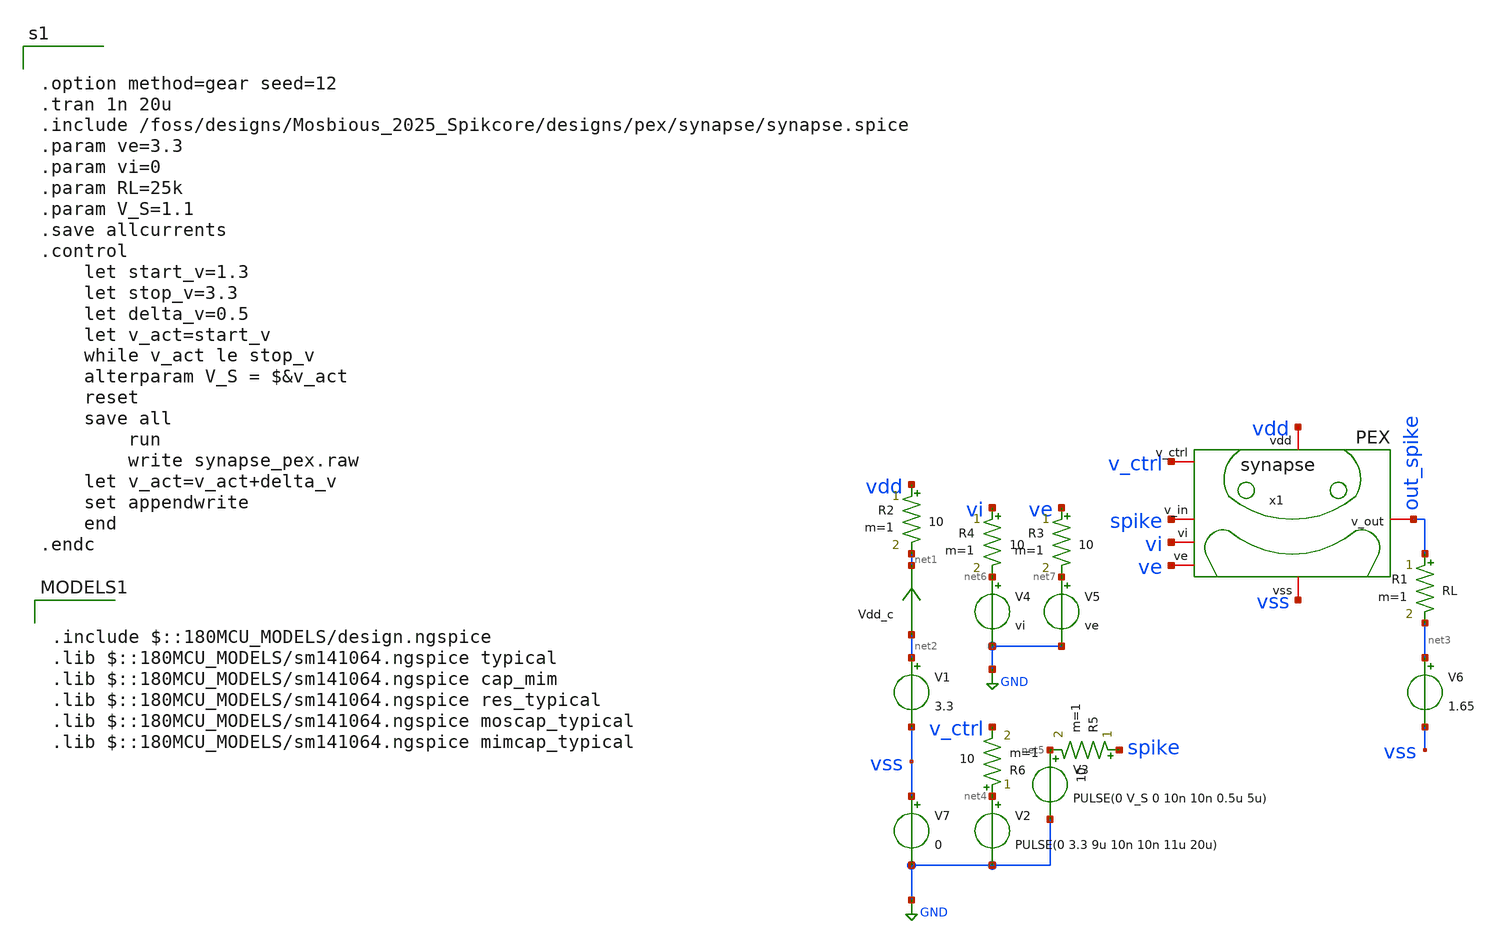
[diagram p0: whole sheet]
** sch_path: designs/pex/synapse/synapse.sch
**.subckt synapse
V1 net2 vss 3.3
Vdd_c net2 net1 0
.save i(vdd_c)
V2 net4 GND PULSE(0 3.3 9u 10n 10n 11u 20u)
V3 net5 GND PULSE(0 V_S 0 10n 10n 0.5u 5u)
V4 net6 GND vi
V5 net7 GND ve
V6 net3 vss 1.65
R1 out_spike net3 RL m=1
R2 vdd net1 10 m=1
R3 ve net7 10 m=1
R4 vi net6 10 m=1
R5 spike net5 10 m=1
R6 net4 v_ctrl 10 m=1
x1 vdd spike ve v_ctrl out_spike vi vss synapse
V7 vss GND 0
**** begin user architecture code


.option method=gear seed=12
.tran 1n 20u
.include /foss/designs/Mosbious_2025_Spikcore/designs/pex/synapse/synapse.spice
.param ve=3.3
.param vi=0
.param RL=25k
.param V_S=1.1
.save allcurrents
.control
    let start_v=1.3
    let stop_v=3.3
    let delta_v=0.5
    let v_act=start_v
    while v_act le stop_v
	alterparam V_S = $&v_act
	reset
	save all
        run
        write synapse_pex.raw
	let v_act=v_act+delta_v
	set appendwrite
    end
.endc



.include $::180MCU_MODELS/design.ngspice
.lib $::180MCU_MODELS/sm141064.ngspice typical
.lib $::180MCU_MODELS/sm141064.ngspice cap_mim
.lib $::180MCU_MODELS/sm141064.ngspice res_typical
.lib $::180MCU_MODELS/sm141064.ngspice moscap_typical
.lib $::180MCU_MODELS/sm141064.ngspice mimcap_typical

**** end user architecture code
**.ends
.GLOBAL GND
.end
